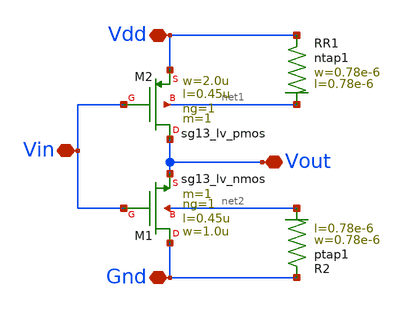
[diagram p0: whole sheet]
** sch_path: modules/module_3_8_bit_SAR_ADC/part_5_layout/components/inverter_example/pex/xschem/inverter.sch
**.subckt inverter Vout Vdd Vin Gnd
*.iopin Vout
*.iopin Vdd
*.iopin Vin
*.iopin Gnd
XM1 Gnd Vin Vout net2 sg13_lv_nmos w=1.0u l=0.45u ng=1 m=1 mm_ok=1
XM2 Vout Vin Vdd net1 sg13_lv_pmos w=2.0u l=0.45u ng=1 m=1 mm_ok=1
XR1 Vdd net1 ntap1 R=262.8 w=0.78e-6 l=0.78e-6
XR2 Gnd net2 ptap1 R=262.8 w=0.78e-6 l=0.78e-6
**.ends
.end
